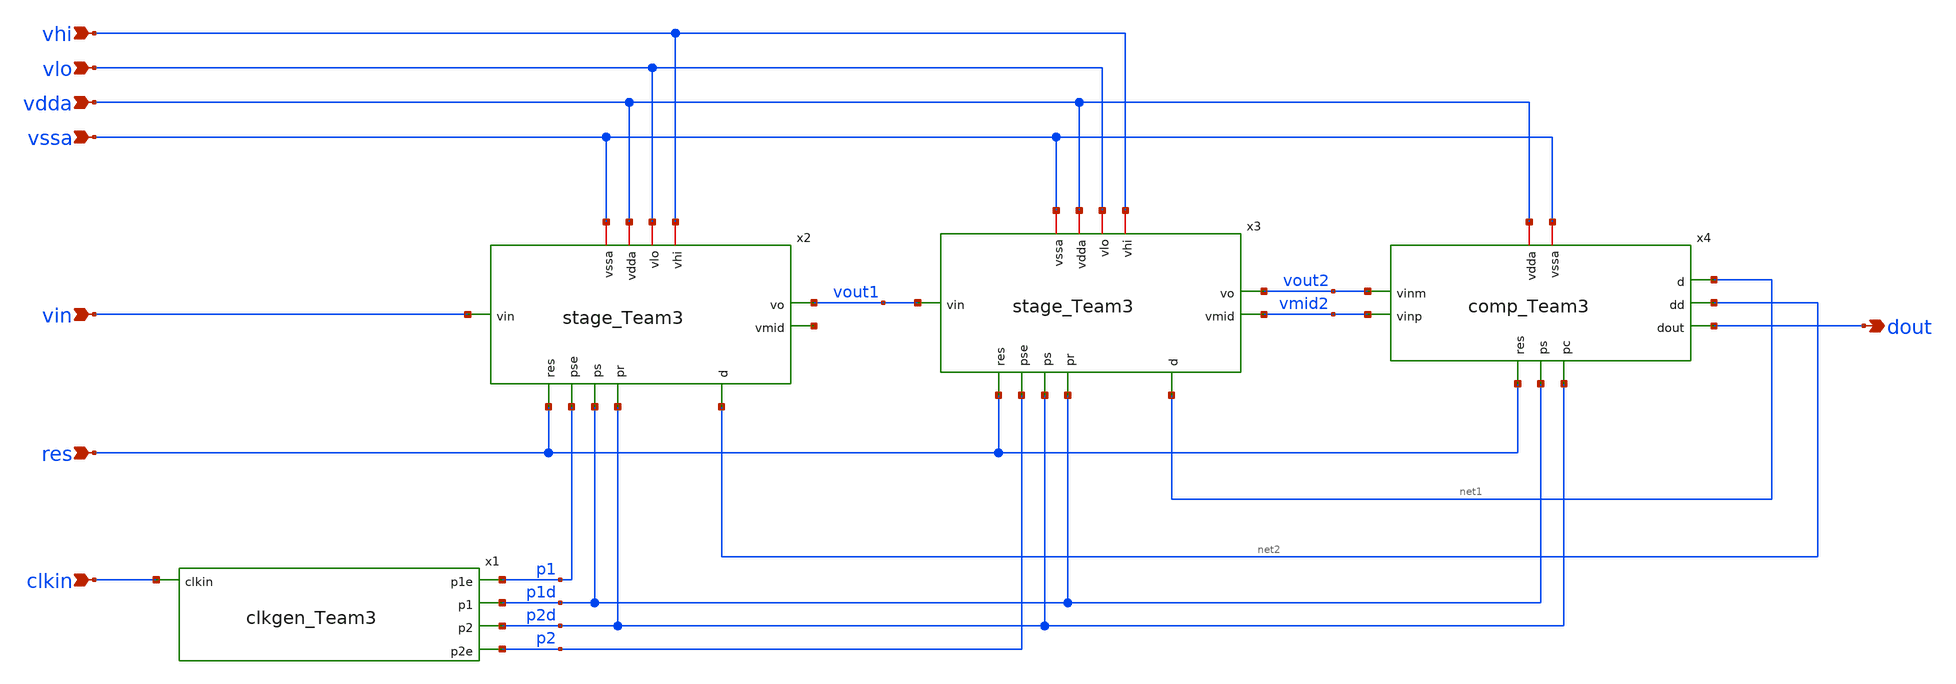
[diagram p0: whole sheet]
** sch_path: 5_Design/4_Layout/Team 3/xschem/idsm2_Team3.sch
* IHP-GmbH/IHP-Open-PDK/ihp-sg13g2/libs.tech/xschem/sg13g2_stdcells/sg13g2_inv_2.sch:
* Copyright 2023 IHP PDK Authors
* Licensed under the Apache License, Version 2.0 (the "License");
**.subckt idsm2_Team3 vhi dout vlo vdda vssa vin clkin res
*.ipin vhi
*.opin dout
*.ipin vlo
*.ipin vdda
*.ipin vssa
*.ipin vin
*.ipin clkin
*.ipin res
x2 res p1 p1d p2d vhi vdda vout1 vin vssa net3 net2 vlo stage_Team3
x3 res p2 p2d p1d vhi vdda vout2 vout1 vssa vmid2 net1 vlo stage_Team3
x4 vdda p2d net1 vmid2 net2 dout vssa res p1d vout2 comp_Team3
x1 p1 clkin p1d p2d p2 clkgen_Team3
**.ends

* expanding   symbol:  /foss/designs/Latest Design/stage_Team3.sym # of pins=12
** sym_path: 5_Design/4_Layout/Team 3/xschem/stage_Team3.sym
** sch_path: 5_Design/4_Layout/Team 3/xschem/stage_Team3.sch
.subckt stage_Team3 res pse ps pr vhi vdda vo vin vssa vmid d vlo
*.ipin res
*.ipin pse
*.ipin ps
*.ipin pr
*.ipin vin
*.iopin vdda
*.opin vo
*.iopin vssa
*.iopin vhi
*.ipin d
*.iopin vlo
*.opin vmid
Xmn1 vssa net4 vo vssa sg13_lv_nmos w=2.5u l=1.5u ng=1 m=1 mm_ok=1
Xmp1 vo net4 vdda vdda sg13_lv_pmos w=10u l=1.5u ng=4 m=1 mm_ok=1
Xmn2 net3 res vo vssa sg13_lv_nmos w=2u l=0.13u ng=1 m=1 mm_ok=1
Xmn3 net4 ps net3 vssa sg13_lv_nmos w=2u l=0.13u ng=1 m=1 mm_ok=1
Xmn4 net2 pr net3 vssa sg13_lv_nmos w=2u l=0.13u ng=1 m=1 mm_ok=1
Xmn5 vmid pse net2 vssa sg13_lv_nmos w=2u l=0.13u ng=1 m=1 mm_ok=1
Xmp2 net1 psb vin vdda sg13_lv_pmos w=6u l=0.13u ng=3 m=1 mm_ok=1
Xmn6 vlo gn net1 vssa sg13_lv_nmos w=0.5u l=0.13u ng=1 m=1 mm_ok=1
Xmn7 vin ps net1 vssa sg13_lv_nmos w=2u l=0.13u ng=1 m=1 mm_ok=1
x1 psb ps VDD VSS sg13g2_inv_1
Xmp3 net1 net5 vhi vdda sg13_lv_pmos w=1.5u l=0.13u ng=1 m=1 mm_ok=1
x3 gn pr d VDD VSS sg13g2_and2_1
Xmn8 vssa vmid vmid vssa sg13_lv_nmos w=2.5u l=1.5u ng=1 m=1 mm_ok=1
Xmp4 vmid vmid vdda vdda sg13_lv_pmos w=10u l=1.5u ng=4 m=1 mm_ok=1
XC4 net2 net1 cap_cmim w=5.77e-6 l=5.77e-6 m=1 mm_ok=1
XC1 net4 net2 cap_cmim w=8.16e-6 l=8.16e-6 m=1 mm_ok=1
XC2 net3 vo cap_cmim w=8.16e-6 l=8.16e-6 m=1 mm_ok=1
x2 net5 d pr VDD VSS sg13g2_nand2b_1
.ends


* expanding   symbol:  /foss/designs/Latest Design/comp_Team3.sym # of pins=10
** sym_path: 5_Design/4_Layout/Team 3/xschem/comp_Team3.sym
** sch_path: 5_Design/4_Layout/Team 3/xschem/comp_Team3.sch
.subckt comp_Team3 vdda pc d vinp dd dout vssa res ps vinm
*.ipin pc
*.iopin vssa
*.iopin vdda
*.ipin vinp
*.ipin vinm
*.opin d
*.ipin res
*.opin dd
*.ipin ps
*.opin dout
XM1 d2p out1p out1m vssa sg13_lv_nmos w=2u l=0.13u ng=1 m=1 mm_ok=1
XM2 out1m out1p vdda vdda sg13_lv_pmos w=4u l=0.13u ng=1 m=1 mm_ok=1
XM3 out1m pc vdda vdda sg13_lv_pmos w=4u l=0.13u ng=1 m=1 mm_ok=1
XM4 d1p pc d2p vssa sg13_lv_nmos w=2u l=0.13u ng=1 m=1 mm_ok=1
XM5 vssa vinp d1p vssa sg13_lv_nmos w=2u l=1u ng=1 m=1 mm_ok=1
XM6 d1m pc d2m vssa sg13_lv_nmos w=2u l=0.13u ng=1 m=1 mm_ok=1
XM7 vssa vinm_samp d1m vssa sg13_lv_nmos w=2u l=1u ng=1 m=1 mm_ok=1
XM8 d2m out1m out1p vssa sg13_lv_nmos w=2u l=0.13u ng=1 m=1 mm_ok=1
XM9 out1p pc vdda vdda sg13_lv_pmos w=4u l=0.13u ng=1 m=1 mm_ok=1
XM10 out1p out1m vdda vdda sg13_lv_pmos w=4u l=0.13u ng=1 m=1 mm_ok=1
XM11 net2 out1p VDD VDD sg13_lv_pmos w=4u l=0.13u ng=1 m=1 mm_ok=1
XM12 net2 net3 VDD VDD sg13_lv_pmos w=4u l=0.13u ng=1 m=1 mm_ok=1
XM13 net3 net2 VDD VDD sg13_lv_pmos w=4u l=0.13u ng=1 m=1 mm_ok=1
XM14 net3 out1m VDD VDD sg13_lv_pmos w=4u l=0.13u ng=1 m=1 mm_ok=1
XM15 net1 net3 net2 VSS sg13_lv_nmos w=2u l=0.13u ng=1 m=1 mm_ok=1
XM16 net4 net2 net3 VSS sg13_lv_nmos w=2u l=0.13u ng=1 m=1 mm_ok=1
XM17 VSS out1p net1 VSS sg13_lv_nmos w=2u l=0.13u ng=1 m=1 mm_ok=1
XM18 VSS out1m net4 VSS sg13_lv_nmos w=2u l=0.13u ng=1 m=1 mm_ok=1
x1 d net3 VDD VSS sg13g2_buf_2
x2 dd net7 ps net3 net5 VDD VSS sg13g2_dfrbp_2
x3 net5 res VDD VSS sg13g2_inv_1
XM19 vinm ps vinm_samp vssa sg13_lv_nmos w=2u l=0.13u ng=1 m=1 mm_ok=1
XM20 vinm_samp net6 vinm vdda sg13_lv_pmos w=6u l=0.13u ng=3 m=1 mm_ok=1
x4 net6 ps VDD VSS sg13g2_inv_1
x5 dout dd VDD VSS sg13g2_inv_2
XC1 vinm_samp vssa cap_cmim w=5.77e-6 l=5.77e-6 m=1 mm_ok=1
.ends


* expanding   symbol:  /foss/designs/Latest Design/clkgen_Team3.sym # of pins=5
** sym_path: 5_Design/4_Layout/Team 3/xschem/clkgen_Team3.sym
** sch_path: 5_Design/4_Layout/Team 3/xschem/clkgen_Team3.sch
.subckt clkgen_Team3 p1e clkin p1 p2 p2e
*.ipin clkin
*.opin p1e
*.opin p2e
*.opin p1
*.opin p2
x7 net1 clkin VDD VSS sg13g2_inv_2
x10 net2 net1 VDD VSS sg13g2_inv_2
x11 net3 net2 net14 VDD VSS sg13g2_nand2_2
x12 net4 net3 VDD VSS sg13g2_inv_4
x13 net5 net4 VDD VSS sg13g2_inv_4
x16 net6 net5 VDD VSS sg13g2_inv_4
x17 net7 net6 VDD VSS sg13g2_inv_4
x18 net10 net9 VDD VSS sg13g2_inv_4
x19 net11 net10 VDD VSS sg13g2_inv_4
x20 net12 net11 VDD VSS sg13g2_inv_4
x21 net13 net12 VDD VSS sg13g2_inv_4
x22 net9 net1 net16 VDD VSS sg13g2_nand2_2
x23 p1e net7 VDD VSS sg13g2_inv_4
x24 net16 p1e VDD VSS sg13g2_inv_4
x25 p2e net13 VDD VSS sg13g2_inv_4
x26 net14 p2e VDD VSS sg13g2_inv_4
x27 net17 net7 net16 VDD VSS sg13g2_nand2_2
x28 net18 net13 net14 VDD VSS sg13g2_nand2_2
x29 net8 net17 VDD VSS sg13g2_inv_4
x30 net15 net18 VDD VSS sg13g2_inv_4
x31 p1 net8 VDD VSS sg13g2_inv_8
x32 p2 net15 VDD VSS sg13g2_inv_8
.ends


* expanding   symbol:  sg13g2_stdcells/sg13g2_inv_1.sym # of pins=2
** sym_path: sg13g2_stdcells/sg13g2_inv_1.sym
** sch_path: sg13g2_stdcells/sg13g2_inv_1.sch
.subckt sg13g2_inv_1 Y A VDD VSS
*.opin Y
*.ipin A
*.iopin VDD
*.iopin VSS
XM1 Y A VSS VSS sg13_lv_nmos w=740.00n l=130.00n ng=1 m=1 mm_ok=1
XM2 Y A VDD VDD sg13_lv_pmos w=1.12u l=130.00n ng=1 m=1 mm_ok=1
.ends


* expanding   symbol:  sg13g2_stdcells/sg13g2_and2_1.sym # of pins=3
** sym_path: sg13g2_stdcells/sg13g2_and2_1.sym
** sch_path: sg13g2_stdcells/sg13g2_and2_1.sch
.subckt sg13g2_and2_1 X A B VDD VSS
*.ipin A
*.ipin B
*.opin X
*.iopin VDD
*.iopin VSS
XM1 net1 A net2 VSS sg13_lv_nmos w=640.00n l=130.00n ng=1 m=1 mm_ok=1
XM2 net2 B VSS VSS sg13_lv_nmos w=640.00n l=130.00n ng=1 m=1 mm_ok=1
XM3 X net1 VSS VSS sg13_lv_nmos w=740.00n l=130.00n ng=1 m=1 mm_ok=1
XM4 net1 B VDD VDD sg13_lv_pmos w=840.00n l=130.00n ng=1 m=1 mm_ok=1
XM5 net1 A VDD VDD sg13_lv_pmos w=840.00n l=130.00n ng=1 m=1 mm_ok=1
XM6 X net1 VDD VDD sg13_lv_pmos w=1.12u l=130.00n ng=1 m=1 mm_ok=1
.ends


* expanding   symbol:  sg13g2_stdcells/sg13g2_nand2b_1.sym # of pins=3
** sym_path: sg13g2_stdcells/sg13g2_nand2b_1.sym
** sch_path: sg13g2_stdcells/sg13g2_nand2b_1.sch
.subckt sg13g2_nand2b_1 Y A_N B VDD VSS
*.opin Y
*.ipin B
*.ipin A_N
*.iopin VDD
*.iopin VSS
XM1 net1 A_N VSS VSS sg13_lv_nmos w=550.00n l=130.00n ng=1 m=1 mm_ok=1
XM2 Y net1 net2 VSS sg13_lv_nmos w=740.00n l=130.00n ng=1 m=1 mm_ok=1
XM3 net2 B VSS VSS sg13_lv_nmos w=740.00n l=130.00n ng=1 m=1 mm_ok=1
XM4 Y B VDD VDD sg13_lv_pmos w=1.12u l=130.00n ng=1 m=1 mm_ok=1
XM5 net1 A_N VDD VDD sg13_lv_pmos w=840.00n l=130.00n ng=1 m=1 mm_ok=1
XM6 Y net1 VDD VDD sg13_lv_pmos w=1.12u l=130.00n ng=1 m=1 mm_ok=1
.ends


* expanding   symbol:  sg13g2_stdcells/sg13g2_buf_2.sym # of pins=2
** sym_path: sg13g2_stdcells/sg13g2_buf_2.sym
** sch_path: sg13g2_stdcells/sg13g2_buf_2.sch
.subckt sg13g2_buf_2 X A VDD VSS
*.ipin A
*.opin X
*.iopin VDD
*.iopin VSS
XM1 net1 A VSS VSS sg13_lv_nmos w=640.00n l=130.00n ng=1 m=1 mm_ok=1
XM2 X net1 VSS VSS sg13_lv_nmos w=1.48u l=130.00n ng=2 m=1 mm_ok=1
XM3 net1 A VDD VDD sg13_lv_pmos w=1.000u l=130.00n ng=1 m=1 mm_ok=1
XM4 X net1 VDD VDD sg13_lv_pmos w=2.24u l=130.00n ng=2 m=1 mm_ok=1
.ends


* expanding   symbol:  sg13g2_stdcells/sg13g2_dfrbp_2.sym # of pins=5
** sym_path: sg13g2_stdcells/sg13g2_dfrbp_2.sym
** sch_path: sg13g2_stdcells/sg13g2_dfrbp_2.sch
.subckt sg13g2_dfrbp_2 Q Q_N CLK D RESET_B VDD VSS
*.ipin D
*.ipin RESET_B
*.ipin CLK
*.opin Q
*.opin Q_N
*.iopin VDD
*.iopin VSS
XM1 Db D net12 VSS sg13_lv_nmos w=420.00n l=130.00n ng=1 m=1 mm_ok=1
XM2 net12 RESET_B VSS VSS sg13_lv_nmos w=420.00n l=130.00n ng=1 m=1 mm_ok=1
XM3 net2 clkneg net11 VSS sg13_lv_nmos w=420.00n l=130.00n ng=1 m=1 mm_ok=1
XM4 net11 net3 VSS VSS sg13_lv_nmos w=420.00n l=130.00n ng=1 m=1 mm_ok=1
XM5 net3 net2 net7 VSS sg13_lv_nmos w=420.00n l=130.00n ng=1 m=1 mm_ok=1
XM6 net7 RESET_B VSS VSS sg13_lv_nmos w=420.00n l=130.00n ng=1 m=1 mm_ok=1
XM7 Q_N net2 VSS VSS sg13_lv_nmos w=1.48u l=130.00n ng=2 m=1 mm_ok=1
XM8 net1 net2 VSS VSS sg13_lv_nmos w=640.00n l=130.00n ng=1 m=1 mm_ok=1
XM9 Q net1 VSS VSS sg13_lv_nmos w=1.48u l=130.00n ng=2 m=1 mm_ok=1
XM10 clkneg CLK VSS VSS sg13_lv_nmos w=740.00n l=130.00n ng=1 m=1 mm_ok=1
XM11 clkpos clkneg VSS VSS sg13_lv_nmos w=740.00n l=130.00n ng=1 m=1 mm_ok=1
XM12 Db clkneg net4 VSS sg13_lv_nmos w=420.00n l=130.00n ng=1 m=1 mm_ok=1
XM13 net4 clkpos net10 VSS sg13_lv_nmos w=420.00n l=130.00n ng=1 m=1 mm_ok=1
XM14 net10 net5 net6 VSS sg13_lv_nmos w=420.00n l=130.00n ng=1 m=1 mm_ok=1
XM15 net6 RESET_B VSS VSS sg13_lv_nmos w=420.00n l=130.00n ng=1 m=1 mm_ok=1
XM16 net5 net4 VSS VSS sg13_lv_nmos w=740.00n l=130.00n ng=1 m=1 mm_ok=1
XM17 net5 clkpos net2 VSS sg13_lv_nmos w=740.00n l=130.00n ng=1 m=1 mm_ok=1
XM18 Db RESET_B VDD VDD sg13_lv_pmos w=420.00n l=130.00n ng=1 m=1 mm_ok=1
XM19 Db D VDD VDD sg13_lv_pmos w=420.00n l=130.00n ng=1 m=1 mm_ok=1
XM20 net9 net3 VDD VDD sg13_lv_pmos w=420.00n l=130.00n ng=1 m=1 mm_ok=1
XM21 net2 clkpos net9 VDD sg13_lv_pmos w=420.00n l=130.00n ng=1 m=1 mm_ok=1
XM22 net3 net2 VDD VDD sg13_lv_pmos w=420.00n l=130.00n ng=1 m=1 mm_ok=1
XM23 net3 RESET_B VDD VDD sg13_lv_pmos w=420.00n l=130.00n ng=1 m=1 mm_ok=1
XM24 Q_N net2 VDD VDD sg13_lv_pmos w=2.24u l=130.00n ng=2 m=1 mm_ok=1
XM25 net1 net2 VDD VDD sg13_lv_pmos w=1.000u l=130.00n ng=1 m=1 mm_ok=1
XM26 Q net1 VDD VDD sg13_lv_pmos w=2.24u l=130.00n ng=2 m=1 mm_ok=1
XM27 clkneg CLK VDD VDD sg13_lv_pmos w=1.12u l=130.00n ng=1 m=1 mm_ok=1
XM28 clkpos clkneg VDD VDD sg13_lv_pmos w=1.12u l=130.00n ng=1 m=1 mm_ok=1
XM29 Db clkpos net4 VDD sg13_lv_pmos w=420.00n l=130.00n ng=1 m=1 mm_ok=1
XM30 net8 net5 VDD VDD sg13_lv_pmos w=420.00n l=130.00n ng=1 m=1 mm_ok=1
XM31 net4 clkneg net8 VDD sg13_lv_pmos w=420.00n l=130.00n ng=1 m=1 mm_ok=1
XM32 net4 RESET_B VDD VDD sg13_lv_pmos w=420.00n l=130.00n ng=1 m=1 mm_ok=1
XM33 net5 net4 VDD VDD sg13_lv_pmos w=1.000u l=130.00n ng=1 m=1 mm_ok=1
XM34 net5 clkneg net2 VDD sg13_lv_pmos w=1.000u l=130.00n ng=1 m=1 mm_ok=1
.ends


* expanding   symbol:  sg13g2_stdcells/sg13g2_inv_2.sym # of pins=2
** sym_path: sg13g2_stdcells/sg13g2_inv_2.sym
** sch_path: sg13g2_stdcells/sg13g2_inv_2.sch
.subckt sg13g2_inv_2 Y A VDD VSS
*.opin Y
*.ipin A
*.iopin VDD
*.iopin VSS
XM1 Y A VSS VSS sg13_lv_nmos w=1.48u l=130.00n ng=2 m=1 mm_ok=1
XM2 Y A VDD VDD sg13_lv_pmos w=2.24u l=130.00n ng=2 m=1 mm_ok=1
.ends


* expanding   symbol:  sg13g2_stdcells/sg13g2_nand2_2.sym # of pins=3
** sym_path: sg13g2_stdcells/sg13g2_nand2_2.sym
** sch_path: sg13g2_stdcells/sg13g2_nand2_2.sch
.subckt sg13g2_nand2_2 Y A B VDD VSS
*.iopin VDD
*.iopin VSS
*.opin Y
*.ipin B
*.ipin A
XM1 Y A net1 VSS sg13_lv_nmos w=1.44u l=130.00n ng=2 m=1 mm_ok=1
XM2 net1 B VSS VSS sg13_lv_nmos w=1.44u l=130.00n ng=2 m=1 mm_ok=1
XM3 Y A VDD VDD sg13_lv_pmos w=2.24u l=130.00n ng=2 m=1 mm_ok=1
XM4 Y B VDD VDD sg13_lv_pmos w=2.24u l=130.00n ng=2 m=1 mm_ok=1
.ends


* expanding   symbol:  sg13g2_stdcells/sg13g2_inv_4.sym # of pins=2
** sym_path: sg13g2_stdcells/sg13g2_inv_4.sym
** sch_path: sg13g2_stdcells/sg13g2_inv_4.sch
.subckt sg13g2_inv_4 Y A VDD VSS
*.ipin A
*.opin Y
*.iopin VDD
*.iopin VSS
XM1 Y A VSS VSS sg13_lv_nmos w=2.96u l=130.00n ng=4 m=1 mm_ok=1
XM2 Y A VDD VDD sg13_lv_pmos w=4.48u l=130.00n ng=4 m=1 mm_ok=1
.ends


* expanding   symbol:  sg13g2_stdcells/sg13g2_inv_8.sym # of pins=2
** sym_path: sg13g2_stdcells/sg13g2_inv_8.sym
** sch_path: sg13g2_stdcells/sg13g2_inv_8.sch
.subckt sg13g2_inv_8 Y A VDD VSS
*.opin Y
*.ipin A
*.iopin VDD
*.iopin VSS
XM1 Y A VSS VSS sg13_lv_nmos w=5.92u l=130.00n ng=8 m=1 mm_ok=1
XM2 Y A VDD VDD sg13_lv_pmos w=8.96u l=130.00n ng=8 m=1 mm_ok=1
.ends

.GLOBAL VDD
.GLOBAL VSS
.end
